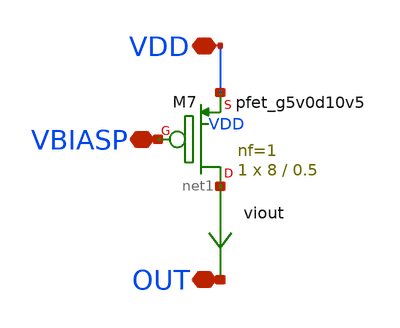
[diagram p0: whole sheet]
** sch_path: xschem/root_currents1outp.sch
**.subckt root_currents1outp VBIASP VDD OUT
*.iopin VBIASP
*.iopin VDD
*.iopin OUT
viout net1 OUT 0
.save i(viout)
XM7 net1 VBIASP VDD VDD sky130_fd_pr__pfet_g5v0d10v5 L=0.5 W=8 nf=1 ad='int((nf+1)/2) * W/nf * 0.29'
+ as='int((nf+2)/2) * W/nf * 0.29' pd='2*int((nf+1)/2) * (W/nf + 0.29)' ps='2*int((nf+2)/2) * (W/nf + 0.29)'
+ nrd='0.29 / W' nrs='0.29 / W' sa=0 sb=0 sd=0 mult=1 m=1
**.ends
.end
